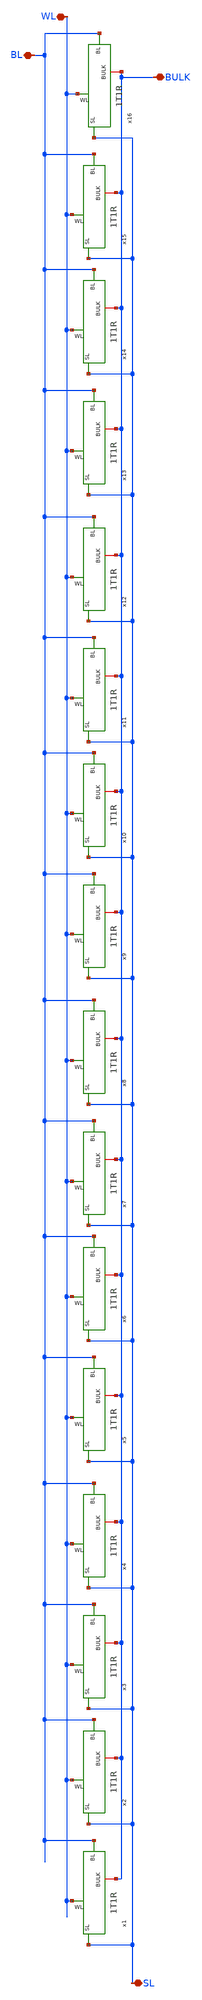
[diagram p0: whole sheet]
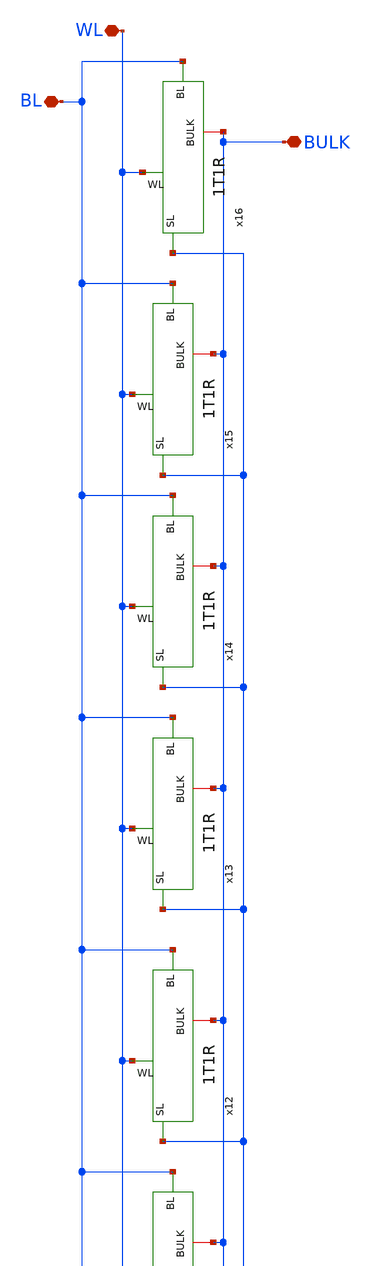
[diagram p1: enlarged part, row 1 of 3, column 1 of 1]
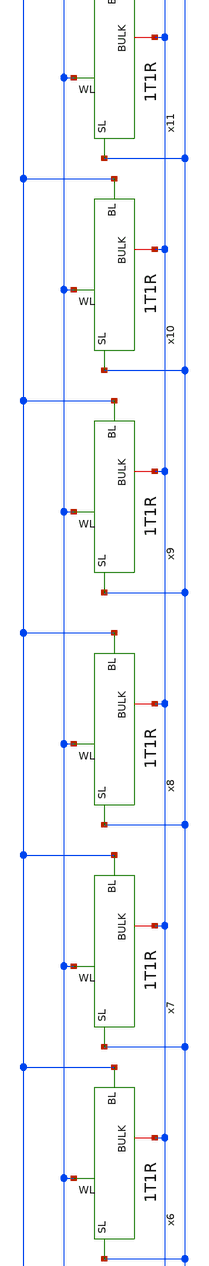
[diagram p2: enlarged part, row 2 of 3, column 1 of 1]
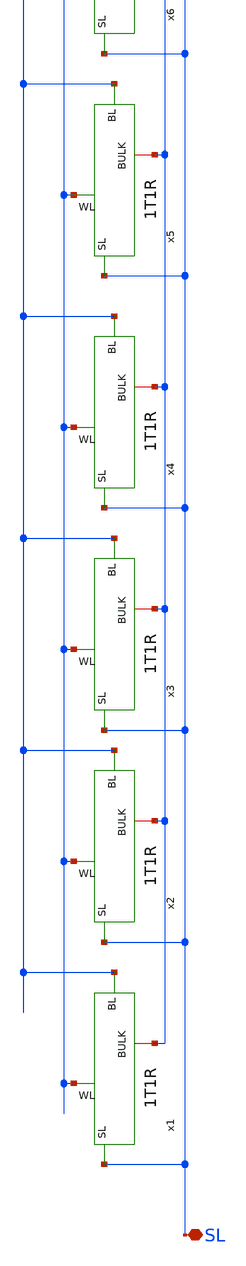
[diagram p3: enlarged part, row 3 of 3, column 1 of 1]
** sch_path: sch/16x1T1R.sch
**.subckt 16x1T1R BL WL SL BULK
*.iopin BL
*.iopin WL
*.iopin SL
*.iopin BULK
x1 BL WL BULK SL 1T1R
x2 BL WL BULK SL 1T1R
x3 BL WL BULK SL 1T1R
x4 BL WL BULK SL 1T1R
x5 BL WL BULK SL 1T1R
x6 BL WL BULK SL 1T1R
x7 BL WL BULK SL 1T1R
x8 BL WL BULK SL 1T1R
x9 BL WL BULK SL 1T1R
x10 BL WL BULK SL 1T1R
x11 BL WL BULK SL 1T1R
x12 BL WL BULK SL 1T1R
x13 BL WL BULK SL 1T1R
x14 BL WL BULK SL 1T1R
x15 BL WL BULK SL 1T1R
x16 BL WL BULK SL 1T1R
**.ends
.end
